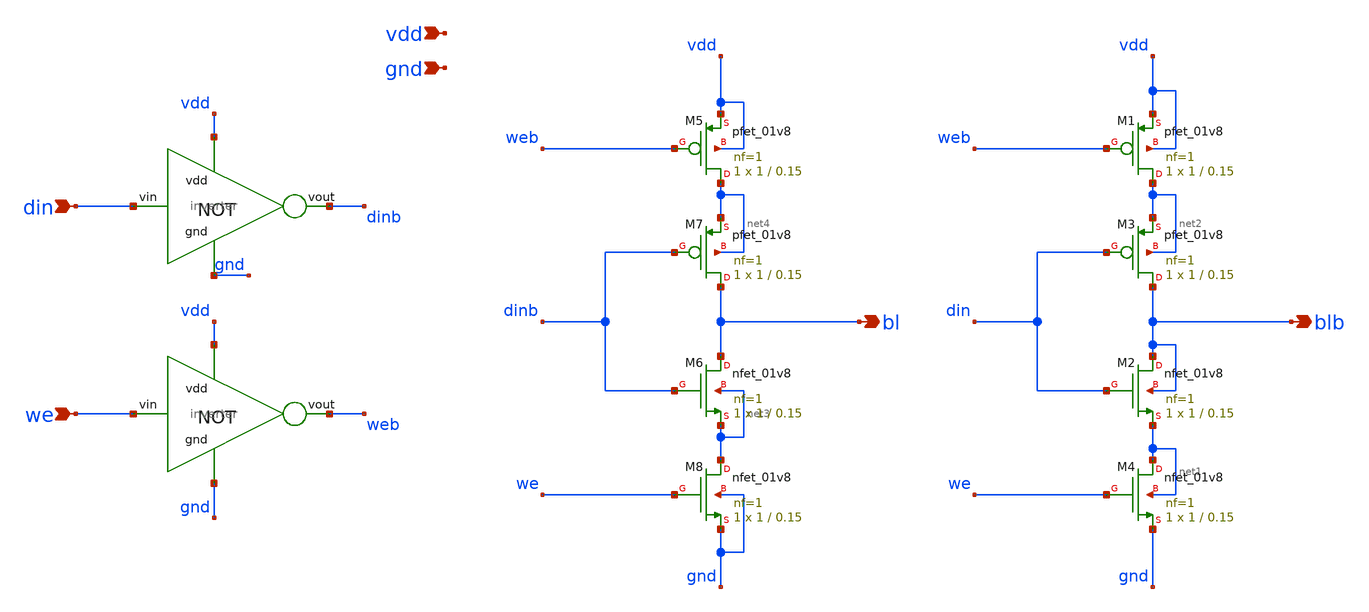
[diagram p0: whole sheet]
** sch_path: sram/write_driver.sch
**.subckt write_driver din we bl blb vdd gnd
*.ipin din
*.ipin we
*.opin bl
*.opin blb
*.ipin vdd
*.ipin gnd
XM1 net2 web vdd vdd sky130_fd_pr__pfet_01v8 L=0.15 W=1 nf=1 ad='int((nf+1)/2) * W/nf * 0.29' as='int((nf+2)/2) * W/nf * 0.29'
+ pd='2*int((nf+1)/2) * (W/nf + 0.29)' ps='2*int((nf+2)/2) * (W/nf + 0.29)' nrd='0.29 / W' nrs='0.29 / W'
+ sa=0 sb=0 sd=0 mult=1 m=1
XM2 blb din net1 blb sky130_fd_pr__nfet_01v8 L=0.15 W=1 nf=1 ad='int((nf+1)/2) * W/nf * 0.29' as='int((nf+2)/2) * W/nf * 0.29'
+ pd='2*int((nf+1)/2) * (W/nf + 0.29)' ps='2*int((nf+2)/2) * (W/nf + 0.29)' nrd='0.29 / W' nrs='0.29 / W'
+ sa=0 sb=0 sd=0 mult=1 m=1
XM3 blb din net2 net2 sky130_fd_pr__pfet_01v8 L=0.15 W=1 nf=1 ad='int((nf+1)/2) * W/nf * 0.29' as='int((nf+2)/2) * W/nf * 0.29'
+ pd='2*int((nf+1)/2) * (W/nf + 0.29)' ps='2*int((nf+2)/2) * (W/nf + 0.29)' nrd='0.29 / W' nrs='0.29 / W'
+ sa=0 sb=0 sd=0 mult=1 m=1
XM4 net1 we gnd net1 sky130_fd_pr__nfet_01v8 L=0.15 W=1 nf=1 ad='int((nf+1)/2) * W/nf * 0.29' as='int((nf+2)/2) * W/nf * 0.29'
+ pd='2*int((nf+1)/2) * (W/nf + 0.29)' ps='2*int((nf+2)/2) * (W/nf + 0.29)' nrd='0.29 / W' nrs='0.29 / W'
+ sa=0 sb=0 sd=0 mult=1 m=1
XM5 net4 web vdd vdd sky130_fd_pr__pfet_01v8 L=0.15 W=1 nf=1 ad='int((nf+1)/2) * W/nf * 0.29' as='int((nf+2)/2) * W/nf * 0.29'
+ pd='2*int((nf+1)/2) * (W/nf + 0.29)' ps='2*int((nf+2)/2) * (W/nf + 0.29)' nrd='0.29 / W' nrs='0.29 / W'
+ sa=0 sb=0 sd=0 mult=1 m=1
XM6 bl dinb net3 net3 sky130_fd_pr__nfet_01v8 L=0.15 W=1 nf=1 ad='int((nf+1)/2) * W/nf * 0.29' as='int((nf+2)/2) * W/nf * 0.29'
+ pd='2*int((nf+1)/2) * (W/nf + 0.29)' ps='2*int((nf+2)/2) * (W/nf + 0.29)' nrd='0.29 / W' nrs='0.29 / W'
+ sa=0 sb=0 sd=0 mult=1 m=1
XM7 bl dinb net4 net4 sky130_fd_pr__pfet_01v8 L=0.15 W=1 nf=1 ad='int((nf+1)/2) * W/nf * 0.29' as='int((nf+2)/2) * W/nf * 0.29'
+ pd='2*int((nf+1)/2) * (W/nf + 0.29)' ps='2*int((nf+2)/2) * (W/nf + 0.29)' nrd='0.29 / W' nrs='0.29 / W'
+ sa=0 sb=0 sd=0 mult=1 m=1
XM8 net3 we gnd gnd sky130_fd_pr__nfet_01v8 L=0.15 W=1 nf=1 ad='int((nf+1)/2) * W/nf * 0.29' as='int((nf+2)/2) * W/nf * 0.29'
+ pd='2*int((nf+1)/2) * (W/nf + 0.29)' ps='2*int((nf+2)/2) * (W/nf + 0.29)' nrd='0.29 / W' nrs='0.29 / W'
+ sa=0 sb=0 sd=0 mult=1 m=1
x1 vdd din dinb gnd inverter
x2 vdd we web gnd inverter
**.ends

* expanding   symbol:  inverter.sym # of pins=4
** sym_path: sram/inverter.sym
** sch_path: sram/inverter.sch
.subckt inverter vdd vin vout gnd
*.ipin vin
*.ipin vdd
*.ipin gnd
*.opin vout
XM1 vout vin gnd gnd sky130_fd_pr__nfet_01v8 L=0.15 W=1 nf=1 ad='int((nf+1)/2) * W/nf * 0.29' as='int((nf+2)/2) * W/nf * 0.29'
+ pd='2*int((nf+1)/2) * (W/nf + 0.29)' ps='2*int((nf+2)/2) * (W/nf + 0.29)' nrd='0.29 / W' nrs='0.29 / W'
+ sa=0 sb=0 sd=0 mult=1 m=1
XM2 vout vin vdd vdd sky130_fd_pr__pfet_01v8 L=0.15 W=1 nf=1 ad='int((nf+1)/2) * W/nf * 0.29' as='int((nf+2)/2) * W/nf * 0.29'
+ pd='2*int((nf+1)/2) * (W/nf + 0.29)' ps='2*int((nf+2)/2) * (W/nf + 0.29)' nrd='0.29 / W' nrs='0.29 / W'
+ sa=0 sb=0 sd=0 mult=1 m=1
.ends

.end
